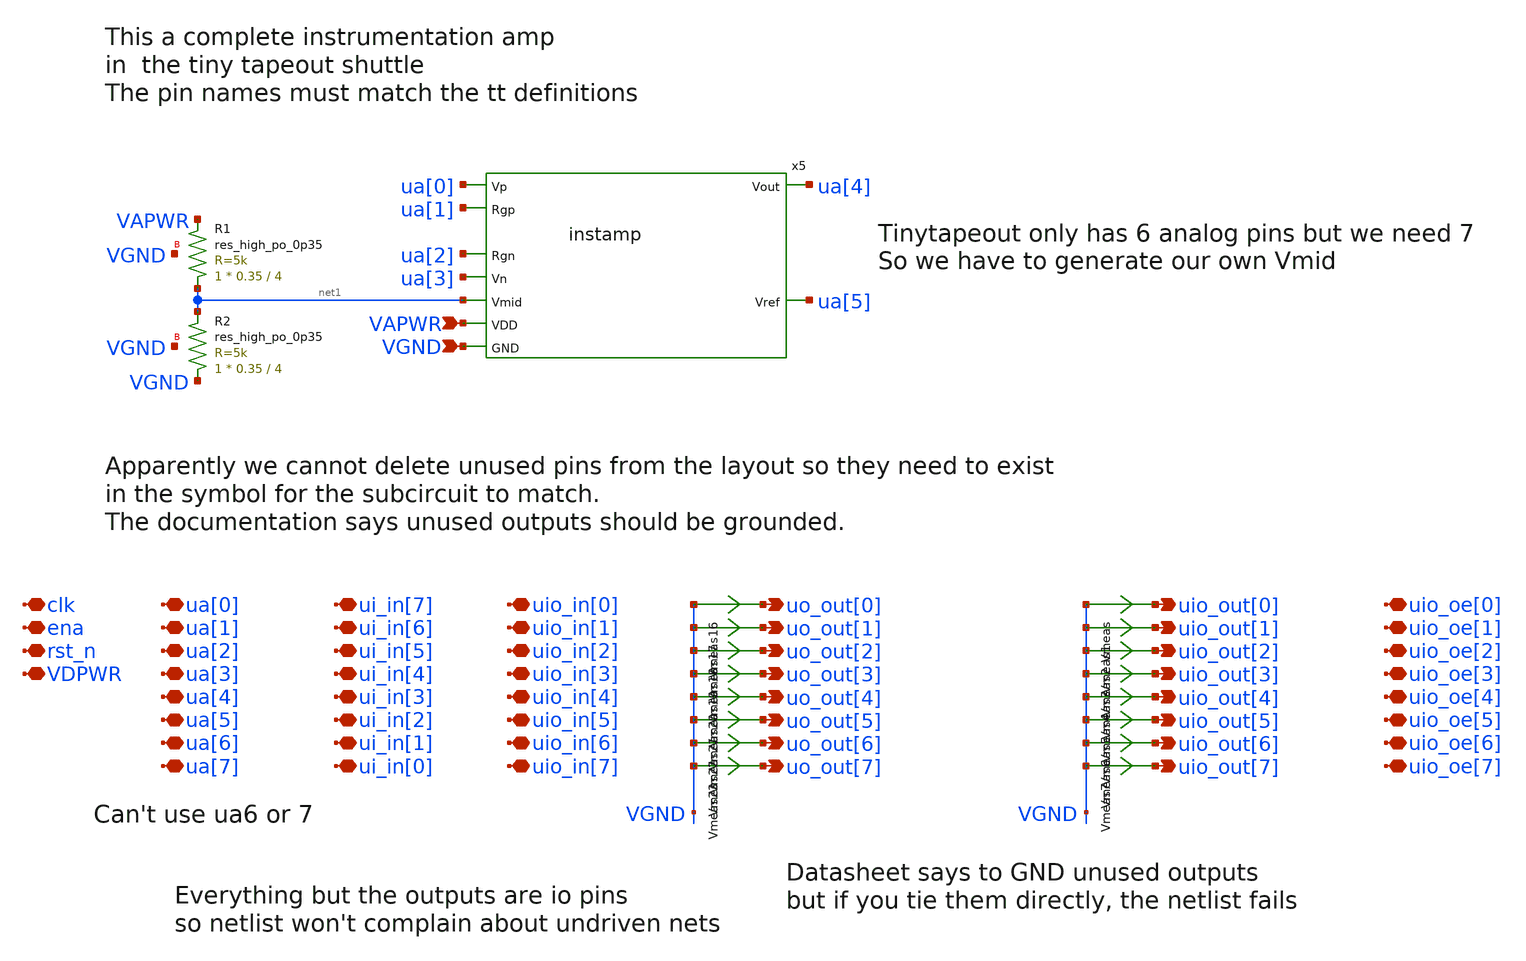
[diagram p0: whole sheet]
** sch_path: xschem/tt_um_jonathanwest3_instamp_sp2026.sch
* Copyright 2021 Stefan Frederik Schippers
* Licensed under the Apache License, Version 2.0 (the "License");
* you may not use this file except in compliance with the License.
* You may obtain a copy of the License at
* https://www.apache.org/licenses/LICENSE-2.0
* Unless required by applicable law or agreed to in writing, software
* distributed under the License is distributed on an "AS IS" BASIS,
* WITHOUT WARRANTIES OR CONDITIONS OF ANY KIND, either express or implied.
* See the License for the specific language governing permissions and
* limitations under the License.
**.subckt tt_um_jonathanwest3_instamp_sp2026 VGND VAPWR uo_out[0] uo_out[1] uo_out[2] uo_out[3]
*+ uo_out[4] uo_out[5] uo_out[6] uo_out[7] uio_out[0] uio_out[1] uio_out[2] uio_out[3] uio_out[4] uio_out[5]
*+ uio_out[6] uio_out[7] ui_in[7] clk ena rst_n VDPWR uio_oe[0] uio_in[0] ui_in[6] ui_in[5] ui_in[4] ui_in[3]
*+ ui_in[2] ui_in[1] ui_in[0] ua[0] ua[1] ua[2] ua[3] ua[4] ua[5] ua[6] ua[7] uio_oe[1] uio_oe[2] uio_oe[3]
*+ uio_oe[4] uio_oe[5] uio_oe[6] uio_oe[7] uio_in[1] uio_in[2] uio_in[3] uio_in[4] uio_in[5] uio_in[6] uio_in[7]
*.ipin VGND
*.ipin VAPWR
*.opin uo_out[0]
*.opin uo_out[1]
*.opin uo_out[2]
*.opin uo_out[3]
*.opin uo_out[4]
*.opin uo_out[5]
*.opin uo_out[6]
*.opin uo_out[7]
*.opin uio_out[0]
*.opin uio_out[1]
*.opin uio_out[2]
*.opin uio_out[3]
*.opin uio_out[4]
*.opin uio_out[5]
*.opin uio_out[6]
*.opin uio_out[7]
*.iopin ui_in[7]
*.iopin clk
*.iopin ena
*.iopin rst_n
*.iopin VDPWR
*.iopin uio_oe[0]
*.iopin uio_in[0]
*.iopin ui_in[6]
*.iopin ui_in[5]
*.iopin ui_in[4]
*.iopin ui_in[3]
*.iopin ui_in[2]
*.iopin ui_in[1]
*.iopin ui_in[0]
*.iopin ua[0]
*.iopin ua[1]
*.iopin ua[2]
*.iopin ua[3]
*.iopin ua[4]
*.iopin ua[5]
*.iopin ua[6]
*.iopin ua[7]
*.iopin uio_oe[1]
*.iopin uio_oe[2]
*.iopin uio_oe[3]
*.iopin uio_oe[4]
*.iopin uio_oe[5]
*.iopin uio_oe[6]
*.iopin uio_oe[7]
*.iopin uio_in[1]
*.iopin uio_in[2]
*.iopin uio_in[3]
*.iopin uio_in[4]
*.iopin uio_in[5]
*.iopin uio_in[6]
*.iopin uio_in[7]
x5 ua[3] ua[2] ua[0] ua[1] net1 ua[4] ua[5] VAPWR VGND instamp
XR1 net1 VAPWR VGND sky130_fd_pr__res_high_po_0p35 L=4 mult=1 m=1
XR2 VGND net1 VGND sky130_fd_pr__res_high_po_0p35 L=4 mult=1 m=1
Vmeas VGND uio_out[0] 0
.save i(vmeas)
Vmeas1 VGND uio_out[1] 0
.save i(vmeas1)
Vmeas2 VGND uio_out[2] 0
.save i(vmeas2)
Vmeas3 VGND uio_out[3] 0
.save i(vmeas3)
Vmeas4 VGND uio_out[4] 0
.save i(vmeas4)
Vmeas5 VGND uio_out[5] 0
.save i(vmeas5)
Vmeas6 VGND uio_out[6] 0
.save i(vmeas6)
Vmeas7 VGND uio_out[7] 0
.save i(vmeas7)
Vmeas16 VGND uo_out[0] 0
.save i(vmeas16)
Vmeas17 VGND uo_out[1] 0
.save i(vmeas17)
Vmeas18 VGND uo_out[2] 0
.save i(vmeas18)
Vmeas19 VGND uo_out[3] 0
.save i(vmeas19)
Vmeas20 VGND uo_out[4] 0
.save i(vmeas20)
Vmeas21 VGND uo_out[5] 0
.save i(vmeas21)
Vmeas22 VGND uo_out[6] 0
.save i(vmeas22)
Vmeas23 VGND uo_out[7] 0
.save i(vmeas23)
**.ends
.end
